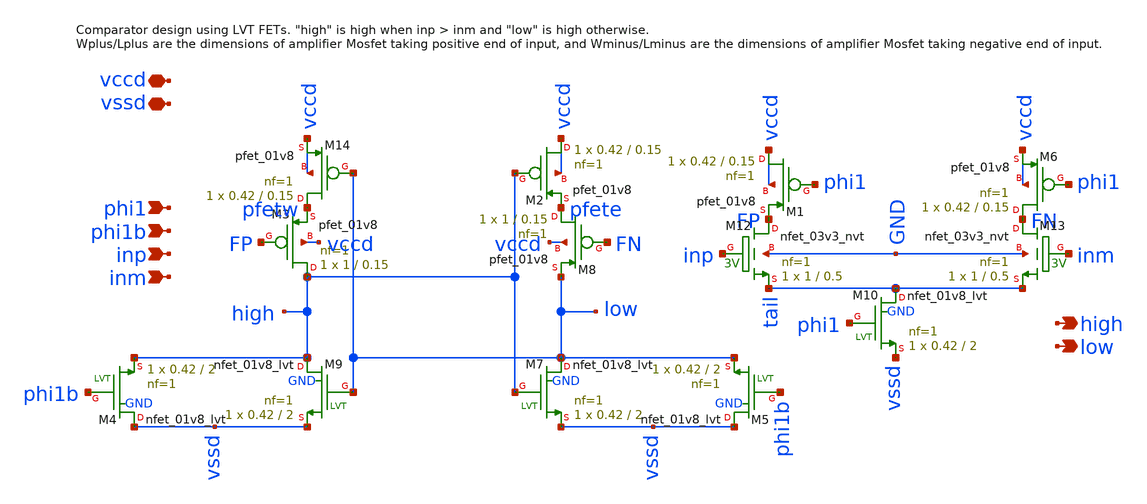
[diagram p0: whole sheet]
** sch_path: xschem/comparator_latest/comparator_single_tail.sch
**.subckt comparator_single_tail phi1 high phi1b inp inm low vccd vssd
*.ipin phi1
*.opin high
*.ipin phi1b
*.ipin inp
*.ipin inm
*.opin low
*.iopin vccd
*.iopin vssd
XM12 FP inp tail GND sky130_fd_pr__nfet_03v3_nvt L=0.5 W=1 nf=1 ad='int((nf+1)/2) * W/nf * 0.29' as='int((nf+2)/2) * W/nf * 0.29'
+ pd='2*int((nf+1)/2) * (W/nf + 0.29)' ps='2*int((nf+2)/2) * (W/nf + 0.29)' nrd='0.29 / W' nrs='0.29 / W'
+ sa=0 sb=0 sd=0 mult=1 m=1
XM13 FN inm tail GND sky130_fd_pr__nfet_03v3_nvt L=0.5 W=1 nf=1 ad='int((nf+1)/2) * W/nf * 0.29' as='int((nf+2)/2) * W/nf * 0.29'
+ pd='2*int((nf+1)/2) * (W/nf + 0.29)' ps='2*int((nf+2)/2) * (W/nf + 0.29)' nrd='0.29 / W' nrs='0.29 / W'
+ sa=0 sb=0 sd=0 mult=1 m=1
XM14 pfetw low vccd vccd sky130_fd_pr__pfet_01v8 L=0.15 W=0.42 nf=1 ad='int((nf+1)/2) * W/nf * 0.29'
+ as='int((nf+2)/2) * W/nf * 0.29' pd='2*int((nf+1)/2) * (W/nf + 0.29)' ps='2*int((nf+2)/2) * (W/nf + 0.29)'
+ nrd='0.29 / W' nrs='0.29 / W' sa=0 sb=0 sd=0 mult=1 m=1
XM3 high FP pfetw vccd sky130_fd_pr__pfet_01v8 L=0.15 W=1 nf=1 ad='int((nf+1)/2) * W/nf * 0.29' as='int((nf+2)/2) * W/nf * 0.29'
+ pd='2*int((nf+1)/2) * (W/nf + 0.29)' ps='2*int((nf+2)/2) * (W/nf + 0.29)' nrd='0.29 / W' nrs='0.29 / W'
+ sa=0 sb=0 sd=0 mult=1 m=1
XM8 pfete FN low vccd sky130_fd_pr__pfet_01v8 L=0.15 W=1 nf=1 ad='int((nf+1)/2) * W/nf * 0.29' as='int((nf+2)/2) * W/nf * 0.29'
+ pd='2*int((nf+1)/2) * (W/nf + 0.29)' ps='2*int((nf+2)/2) * (W/nf + 0.29)' nrd='0.29 / W' nrs='0.29 / W'
+ sa=0 sb=0 sd=0 mult=1 m=1
XM2 vccd high pfete vccd sky130_fd_pr__pfet_01v8 L=0.15 W=0.42 nf=1 ad='int((nf+1)/2) * W/nf * 0.29'
+ as='int((nf+2)/2) * W/nf * 0.29' pd='2*int((nf+1)/2) * (W/nf + 0.29)' ps='2*int((nf+2)/2) * (W/nf + 0.29)'
+ nrd='0.29 / W' nrs='0.29 / W' sa=0 sb=0 sd=0 mult=1 m=1
XM5 vssd phi1b low GND sky130_fd_pr__nfet_01v8_lvt L=2 W=0.42 nf=1 ad='int((nf+1)/2) * W/nf * 0.29' as='int((nf+2)/2) * W/nf * 0.29'
+ pd='2*int((nf+1)/2) * (W/nf + 0.29)' ps='2*int((nf+2)/2) * (W/nf + 0.29)' nrd='0.29 / W' nrs='0.29 / W'
+ sa=0 sb=0 sd=0 mult=1 m=1
XM4 vssd phi1b high GND sky130_fd_pr__nfet_01v8_lvt L=2 W=0.42 nf=1 ad='int((nf+1)/2) * W/nf * 0.29'
+ as='int((nf+2)/2) * W/nf * 0.29' pd='2*int((nf+1)/2) * (W/nf + 0.29)' ps='2*int((nf+2)/2) * (W/nf + 0.29)'
+ nrd='0.29 / W' nrs='0.29 / W' sa=0 sb=0 sd=0 mult=1 m=1
XM7 low high vssd GND sky130_fd_pr__nfet_01v8_lvt L=2 W=0.42 nf=1 ad='int((nf+1)/2) * W/nf * 0.29' as='int((nf+2)/2) * W/nf * 0.29'
+ pd='2*int((nf+1)/2) * (W/nf + 0.29)' ps='2*int((nf+2)/2) * (W/nf + 0.29)' nrd='0.29 / W' nrs='0.29 / W'
+ sa=0 sb=0 sd=0 mult=1 m=1
XM9 high low vssd GND sky130_fd_pr__nfet_01v8_lvt L=2 W=0.42 nf=1 ad='int((nf+1)/2) * W/nf * 0.29' as='int((nf+2)/2) * W/nf * 0.29'
+ pd='2*int((nf+1)/2) * (W/nf + 0.29)' ps='2*int((nf+2)/2) * (W/nf + 0.29)' nrd='0.29 / W' nrs='0.29 / W'
+ sa=0 sb=0 sd=0 mult=1 m=1
XM10 tail phi1 vssd GND sky130_fd_pr__nfet_01v8_lvt L=2 W=0.42 nf=1 ad='int((nf+1)/2) * W/nf * 0.29'
+ as='int((nf+2)/2) * W/nf * 0.29' pd='2*int((nf+1)/2) * (W/nf + 0.29)' ps='2*int((nf+2)/2) * (W/nf + 0.29)'
+ nrd='0.29 / W' nrs='0.29 / W' sa=0 sb=0 sd=0 mult=1 m=1
XM1 vccd phi1 FP vccd sky130_fd_pr__pfet_01v8 L=0.15 W=0.42 nf=1 ad='int((nf+1)/2) * W/nf * 0.29' as='int((nf+2)/2) * W/nf * 0.29'
+ pd='2*int((nf+1)/2) * (W/nf + 0.29)' ps='2*int((nf+2)/2) * (W/nf + 0.29)' nrd='0.29 / W' nrs='0.29 / W'
+ sa=0 sb=0 sd=0 mult=1 m=1
XM6 FN phi1 vccd vccd sky130_fd_pr__pfet_01v8 L=0.15 W=0.42 nf=1 ad='int((nf+1)/2) * W/nf * 0.29' as='int((nf+2)/2) * W/nf * 0.29'
+ pd='2*int((nf+1)/2) * (W/nf + 0.29)' ps='2*int((nf+2)/2) * (W/nf + 0.29)' nrd='0.29 / W' nrs='0.29 / W'
+ sa=0 sb=0 sd=0 mult=1 m=1
**.ends
.end
